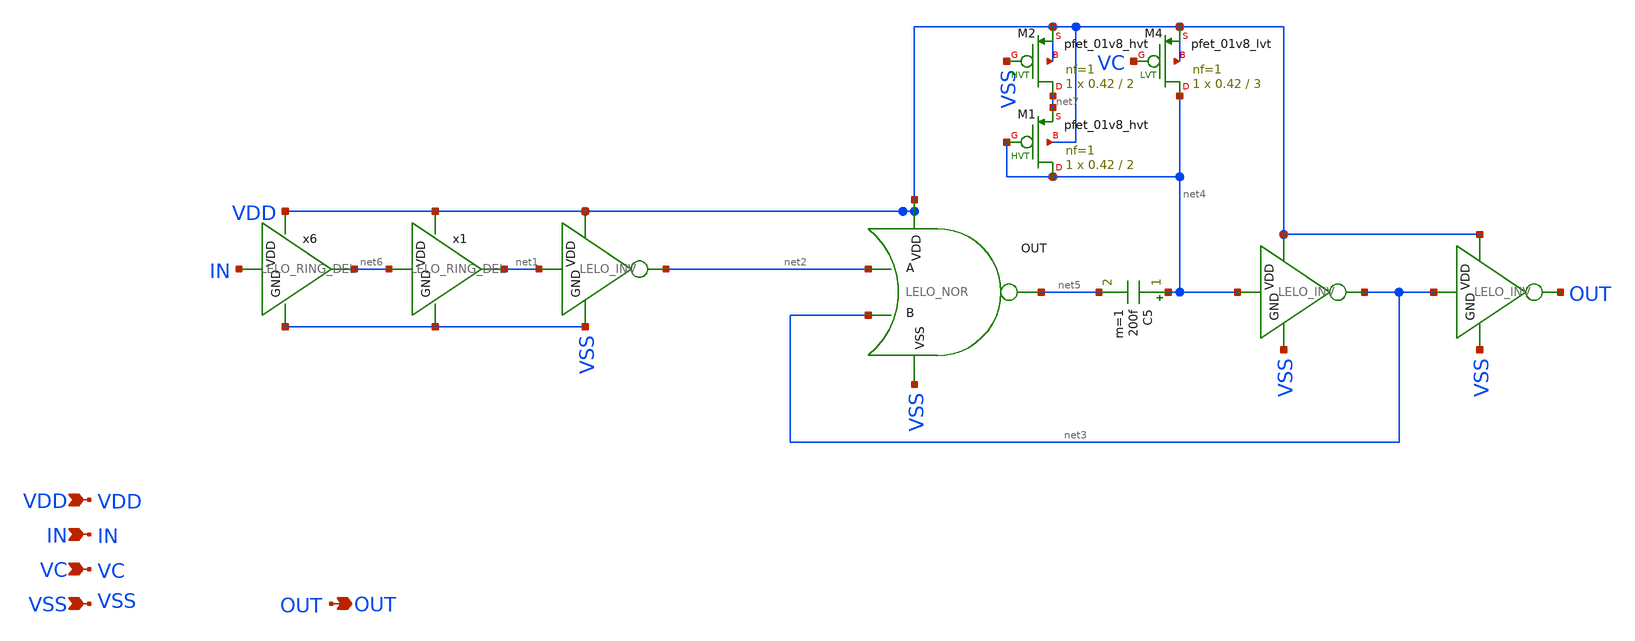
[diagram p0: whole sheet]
** sch_path: design/LELO_SVOD_SKY130A/LELO_ONESHOT_VC.sch
**.subckt LELO_ONESHOT_VC VDD IN VC VSS OUT
*.ipin VDD
*.ipin IN
*.ipin VC
*.ipin VSS
*.opin OUT
x16 VDD net3 OUT VSS LELO_INV
x9 VDD net1 net2 VSS LELO_INV
x2 VDD net5 net2 net3 VSS LELO_NOR
C5 net4 net5 200f m=1
x3 VDD net4 net3 VSS LELO_INV
x1 VDD net6 net1 VSS LELO_RING_DEL
x6 VDD IN net6 VSS LELO_RING_DEL
XM4 net4 VC VDD VDD sky130_fd_pr__pfet_01v8_lvt L=3 W=0.42 nf=1 ad='int((1 + 1)/2) * 0.42 / 1 * 0.29'
+ as='int((1 + 2)/2) * 0.42 / 1 * 0.29' pd='2*int((1 + 1)/2) * (0.42 / 1 + 0.29)' ps='2*int((1 + 2)/2) * (0.42 / 1 + 0.29)'
+ nrd='0.29 / 0.42 ' nrs='0.29 / 0.42 ' sa=0 sb=0 sd=0 mult=1 m=1
XM1 net4 net4 net7 VDD sky130_fd_pr__pfet_01v8_hvt L=2 W=0.42 nf=1 ad='int((1 + 1)/2) * 0.42 / 1 * 0.29'
+ as='int((1 + 2)/2) * 0.42 / 1 * 0.29' pd='2*int((1 + 1)/2) * (0.42 / 1 + 0.29)' ps='2*int((1 + 2)/2) * (0.42 / 1 + 0.29)'
+ nrd='0.29 / 0.42 ' nrs='0.29 / 0.42 ' sa=0 sb=0 sd=0 mult=1 m=1
XM2 net7 VSS VDD VDD sky130_fd_pr__pfet_01v8_hvt L=2 W=0.42 nf=1 ad='int((1 + 1)/2) * 0.42 / 1 * 0.29'
+ as='int((1 + 2)/2) * 0.42 / 1 * 0.29' pd='2*int((1 + 1)/2) * (0.42 / 1 + 0.29)' ps='2*int((1 + 2)/2) * (0.42 / 1 + 0.29)'
+ nrd='0.29 / 0.42 ' nrs='0.29 / 0.42 ' sa=0 sb=0 sd=0 mult=1 m=1
**.ends

* expanding   symbol:  LELO_SVOD_SKY130A/LELO_INV.sym # of pins=4
** sym_path: design/LELO_SVOD_SKY130A/LELO_INV.sym
** sch_path: design/LELO_SVOD_SKY130A/LELO_INV.sch
.subckt LELO_INV VDD VIN VOUT GND
*.ipin VIN
*.ipin VDD
*.ipin GND
*.opin VOUT
XM2 VOUT VIN GND GND sky130_fd_pr__nfet_01v8 L=0.15 W=0.42 nf=1 ad='int((1 + 1)/2) * 0.42 / 1 * 0.29'
+ as='int((1 + 2)/2) * 0.42 / 1 * 0.29' pd='2*int((1 + 1)/2) * (0.42 / 1 + 0.29)' ps='2*int((1 + 2)/2) * (0.42 / 1 + 0.29)'
+ nrd='0.29 / 0.42 ' nrs='0.29 / 0.42 ' sa=0 sb=0 sd=0 mult=1 m=1
XM1 VOUT VIN VDD VDD sky130_fd_pr__pfet_01v8_hvt L=0.15 W=0.42 nf=1 ad='int((1 + 1)/2) * 0.42 / 1 * 0.29'
+ as='int((1 + 2)/2) * 0.42 / 1 * 0.29' pd='2*int((1 + 1)/2) * (0.42 / 1 + 0.29)' ps='2*int((1 + 2)/2) * (0.42 / 1 + 0.29)'
+ nrd='0.29 / 0.42 ' nrs='0.29 / 0.42 ' sa=0 sb=0 sd=0 mult=1 m=1
.ends


* expanding   symbol:  LELO_SVOD_SKY130A/LELO_NOR.sym # of pins=5
** sym_path: design/LELO_SVOD_SKY130A/LELO_NOR.sym
** sch_path: design/LELO_SVOD_SKY130A/LELO_NOR.sch
.subckt LELO_NOR VDD OUT A B VSS
*.ipin VDD
*.ipin VSS
*.opin OUT
*.ipin A
*.ipin B
XM1 OUT B VSS VSS sky130_fd_pr__nfet_01v8 L=0.15 W=0.42 nf=1 ad='int((1 + 1)/2) * 0.42 / 1 * 0.29' as='int((1 + 2)/2) * 0.42 / 1 * 0.29'
+ pd='2*int((1 + 1)/2) * (0.42 / 1 + 0.29)' ps='2*int((1 + 2)/2) * (0.42 / 1 + 0.29)' nrd='0.29 / 0.42 '
+ nrs='0.29 / 0.42 ' sa=0 sb=0 sd=0 mult=1 m=1
XM2 OUT A VSS VSS sky130_fd_pr__nfet_01v8 L=0.15 W=0.42 nf=1 ad='int((1 + 1)/2) * 0.42 / 1 * 0.29' as='int((1 + 2)/2) * 0.42 / 1 * 0.29'
+ pd='2*int((1 + 1)/2) * (0.42 / 1 + 0.29)' ps='2*int((1 + 2)/2) * (0.42 / 1 + 0.29)' nrd='0.29 / 0.42 '
+ nrs='0.29 / 0.42 ' sa=0 sb=0 sd=0 mult=1 m=1
XM3 OUT B net1 VDD sky130_fd_pr__pfet_01v8_hvt L=0.15 W=1 nf=1 ad='int((1 + 1)/2) * 1 / 1 * 0.29' as='int((1 + 2)/2) * 1 / 1 * 0.29'
+ pd='2*int((1 + 1)/2) * (1 / 1 + 0.29)' ps='2*int((1 + 2)/2) * (1 / 1 + 0.29)' nrd='0.29 / 1 ' nrs='0.29 / 1 '
+ sa=0 sb=0 sd=0 mult=1 m=1
XM4 net1 A VDD VDD sky130_fd_pr__pfet_01v8_hvt L=0.15 W=1 nf=1 ad='int((1 + 1)/2) * 1 / 1 * 0.29' as='int((1 + 2)/2) * 1 / 1 * 0.29'
+ pd='2*int((1 + 1)/2) * (1 / 1 + 0.29)' ps='2*int((1 + 2)/2) * (1 / 1 + 0.29)' nrd='0.29 / 1 ' nrs='0.29 / 1 '
+ sa=0 sb=0 sd=0 mult=1 m=1
.ends


* expanding   symbol:  LELO_SVOD_SKY130A/LELO_RING_DEL.sym # of pins=4
** sym_path: design/LELO_SVOD_SKY130A/LELO_RING_DEL.sym
** sch_path: design/LELO_SVOD_SKY130A/LELO_RING_DEL.sch
.subckt LELO_RING_DEL VDD VIN VOUT GND
*.ipin VIN
*.ipin VDD
*.ipin GND
*.opin VOUT
XM1 VOUT VIN GND GND sky130_fd_pr__nfet_01v8_lvt L=1 W=0.42 nf=1 ad='int((1 + 1)/2) * 0.42 / 1 * 0.29'
+ as='int((1 + 2)/2) * 0.42 / 1 * 0.29' pd='2*int((1 + 1)/2) * (0.42 / 1 + 0.29)' ps='2*int((1 + 2)/2) * (0.42 / 1 + 0.29)'
+ nrd='0.29 / 0.42 ' nrs='0.29 / 0.42 ' sa=0 sb=0 sd=0 mult=1 m=1
XM2 VOUT VIN VDD VDD sky130_fd_pr__pfet_01v8_lvt L=1 W=0.42 nf=1 ad='int((1 + 1)/2) * 0.42 / 1 * 0.29'
+ as='int((1 + 2)/2) * 0.42 / 1 * 0.29' pd='2*int((1 + 1)/2) * (0.42 / 1 + 0.29)' ps='2*int((1 + 2)/2) * (0.42 / 1 + 0.29)'
+ nrd='0.29 / 0.42 ' nrs='0.29 / 0.42 ' sa=0 sb=0 sd=0 mult=1 m=1
.ends

.end
